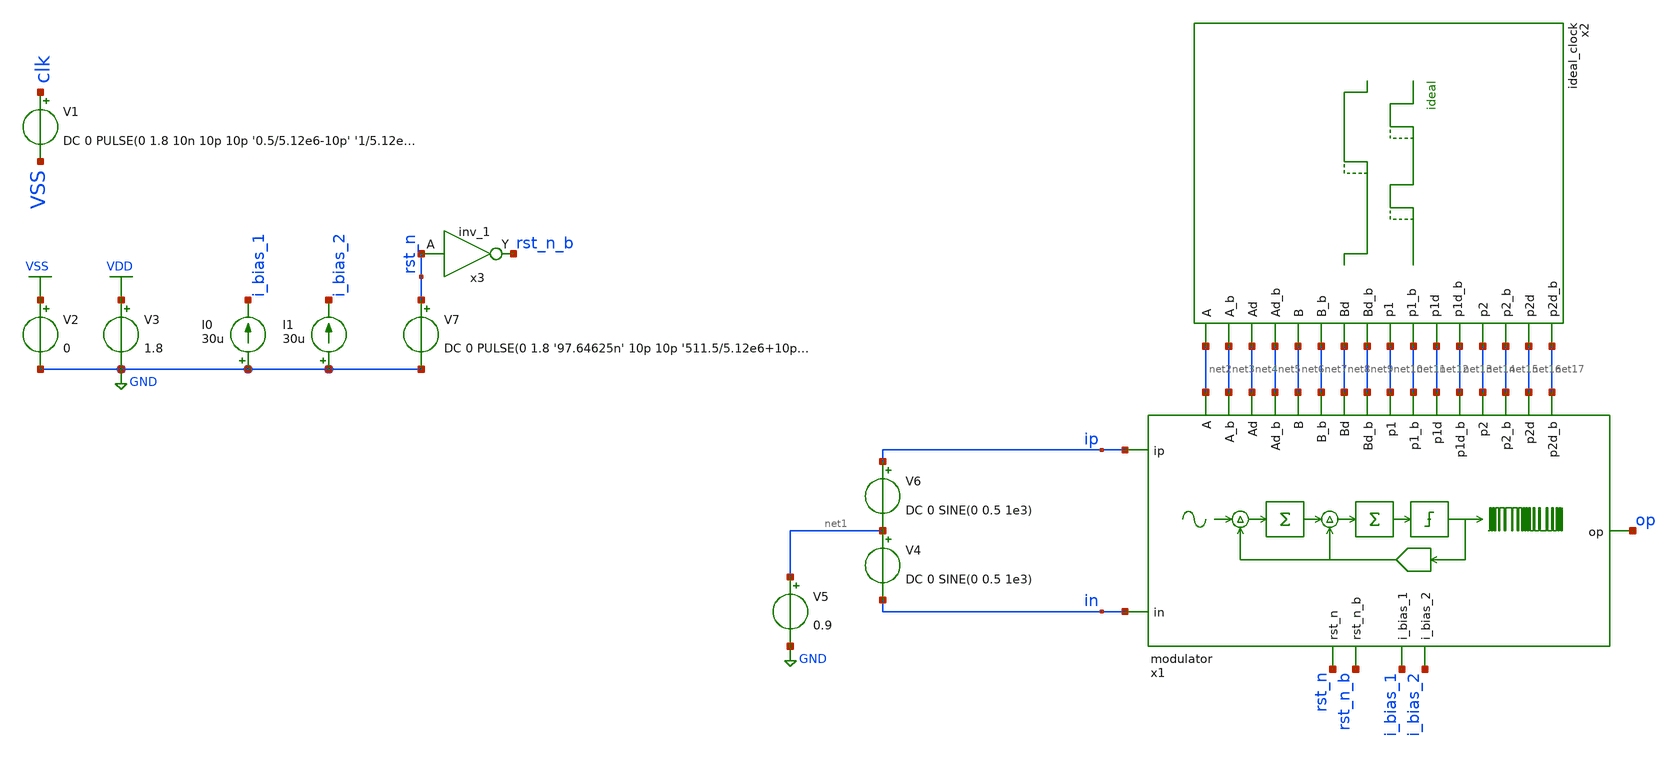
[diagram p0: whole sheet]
** sch_path: verification/schematic_sim/modulator_tb_ideal_clock.sch
**.subckt modulator_tb_ideal_clock
V1 clk VSS DC 0 PULSE(0 1.8 10n 10p 10p '0.5/5.12e6-10p' '1/5.12e6')
V2 VSS GND 0
V3 VDD GND 1.8
I0 GND i_bias_1 30u
I1 GND i_bias_2 30u
V5 net1 GND 0.9
V6 ip net1 DC 0 SINE(0 0.5 1e3)
V4 net1 in DC 0 SINE(0 0.5 1e3)
x3 rst_n GND GND VDD VDD rst_n_b sky130_fd_sc_hd__inv_1
V7 rst_n GND DC 0 PULSE(0 1.8 '97.64625n' 10p 10p '511.5/5.12e6+10p' '512/5.12e6')
x2 net2 net3 net4 net5 net9 net8 net7 net6 net14 net15 net16 net17 net13 net12 net11 net10 97.64625n
+ VDD VSS ideal_clock
x1 ip in net2 net3 net4 net5 net6 net7 net8 net9 net10 net11 net12 net13 net14 net15 net16 net17
+ rst_n rst_n_b i_bias_1 i_bias_2 op VDD VSS modulator
**** begin user architecture code

** opencircuitdesign pdks install
.lib /farmshare/home/classes/ee/372/PDKs/open_pdks_1.0.310/sky130/sky130A/libs.tech/ngspice/sky130.lib.spice tt
.inc /farmshare/home/classes/ee/372/PDKs/open_pdks_1.0.310/sky130/sky130A/libs.ref/sky130_fd_sc_hd/spice/sky130_fd_sc_hd.spice



.control
tran 1u 10m uic
save op
write modulator_tb_ideal_clock.raw v(op)
.endc


**** end user architecture code
**.ends
.GLOBAL GND
.GLOBAL VDD
.GLOBAL VSS
.end
